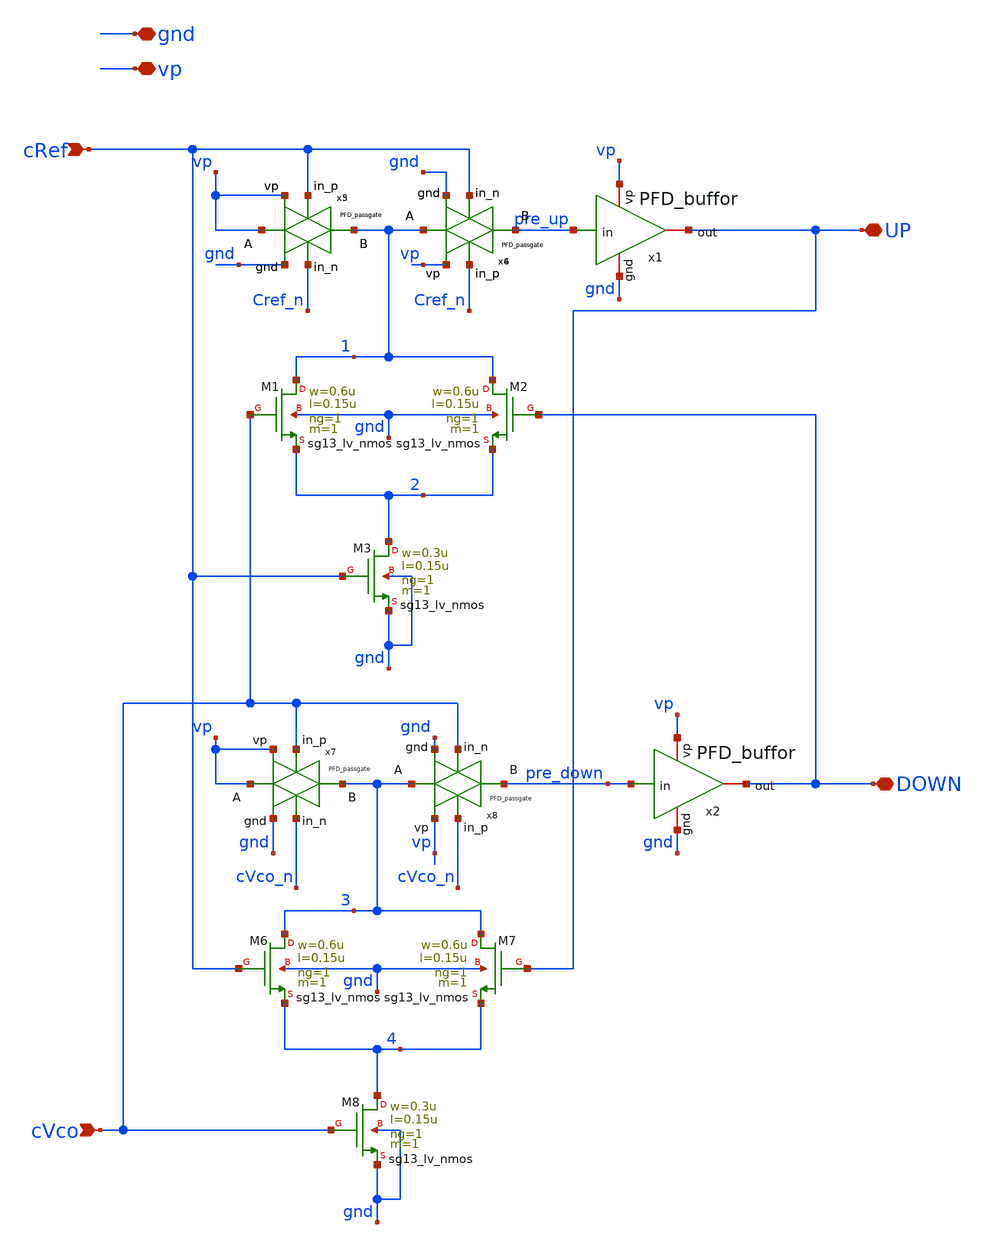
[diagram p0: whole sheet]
** sch_path: PFD/PFD_cell.sch
**.subckt PFD_cell gnd vp DOWN UP cRef cVco
*.iopin gnd
*.iopin vp
*.iopin DOWN
*.iopin UP
*.ipin cRef
*.ipin cVco
XM1 1 cVco 2 gnd sg13_lv_nmos w=0.6u l=0.15u ng=1 m=1 mm_ok=1
XM2 1 DOWN 2 gnd sg13_lv_nmos w=0.6u l=0.15u ng=1 m=1 mm_ok=1
XM3 2 cRef gnd gnd sg13_lv_nmos w=0.3u l=0.15u ng=1 m=1 mm_ok=1
XM6 3 cRef 4 gnd sg13_lv_nmos w=0.6u l=0.15u ng=1 m=1 mm_ok=1
XM7 3 UP 4 gnd sg13_lv_nmos w=0.6u l=0.15u ng=1 m=1 mm_ok=1
XM8 4 cVco gnd gnd sg13_lv_nmos w=0.3u l=0.15u ng=1 m=1 mm_ok=1
x1 gnd vp UP pre_up PFD_buffor
x2 gnd vp DOWN pre_down PFD_buffor
x3 Cref_n vp vp 1 gnd cRef PFD_passgate
x4 cRef vp 1 pre_up gnd Cref_n PFD_passgate
x5 Cref_n vp vp 1 gnd cRef PFD_passgate
x6 cRef vp 1 pre_up gnd Cref_n PFD_passgate
x7 cVco_n vp vp 3 gnd cVco PFD_passgate
x8 cVco vp 3 pre_down gnd cVco_n PFD_passgate
**.ends
.end
